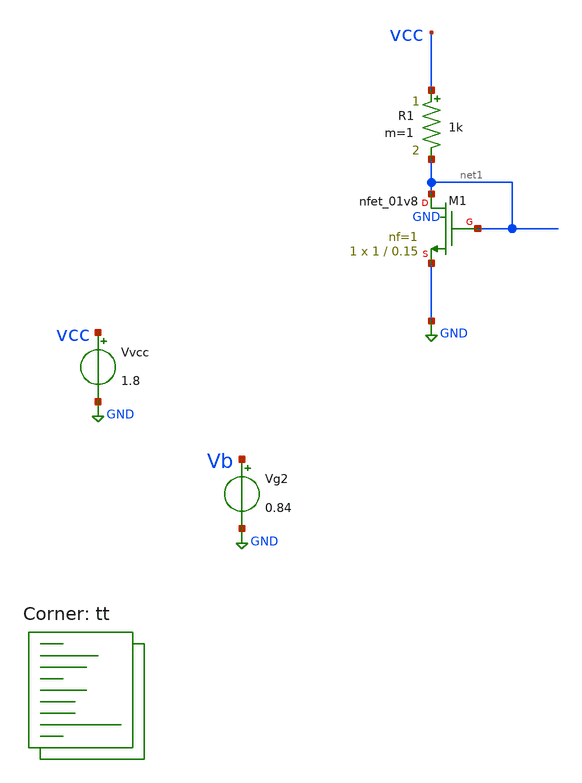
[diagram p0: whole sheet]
** sch_path: xschem/08-learn.sch
**.subckt 08-learn
Vvcc vcc GND 1.8
Vg2 Vb GND 0.84
XM1 net1 net1 GND GND sky130_fd_pr__nfet_01v8 L=0.15 W=1 nf=1 ad='int((nf+1)/2) * W/nf * 0.29' as='int((nf+2)/2) * W/nf * 0.29'
+ pd='2*int((nf+1)/2) * (W/nf + 0.29)' ps='2*int((nf+2)/2) * (W/nf + 0.29)' nrd='0.29 / W' nrs='0.29 / W'
+ sa=0 sb=0 sd=0 mult=1 m=1
R1 vcc net1 1k m=1
**** begin user architecture code



.options savecurrents
.control

  save all
  tran 1n 12.8u
  write 07.raw v(Vb) i(va1) i(va2) i(va3) i(va4) i(va5)
  plot i(va1) i(va2) i(va3) i(va4) i(va5)

.endc



.lib $::SKYWATER_MODELS/sky130.lib.spice tt
**** end user architecture code
**.ends
.GLOBAL GND
.end
